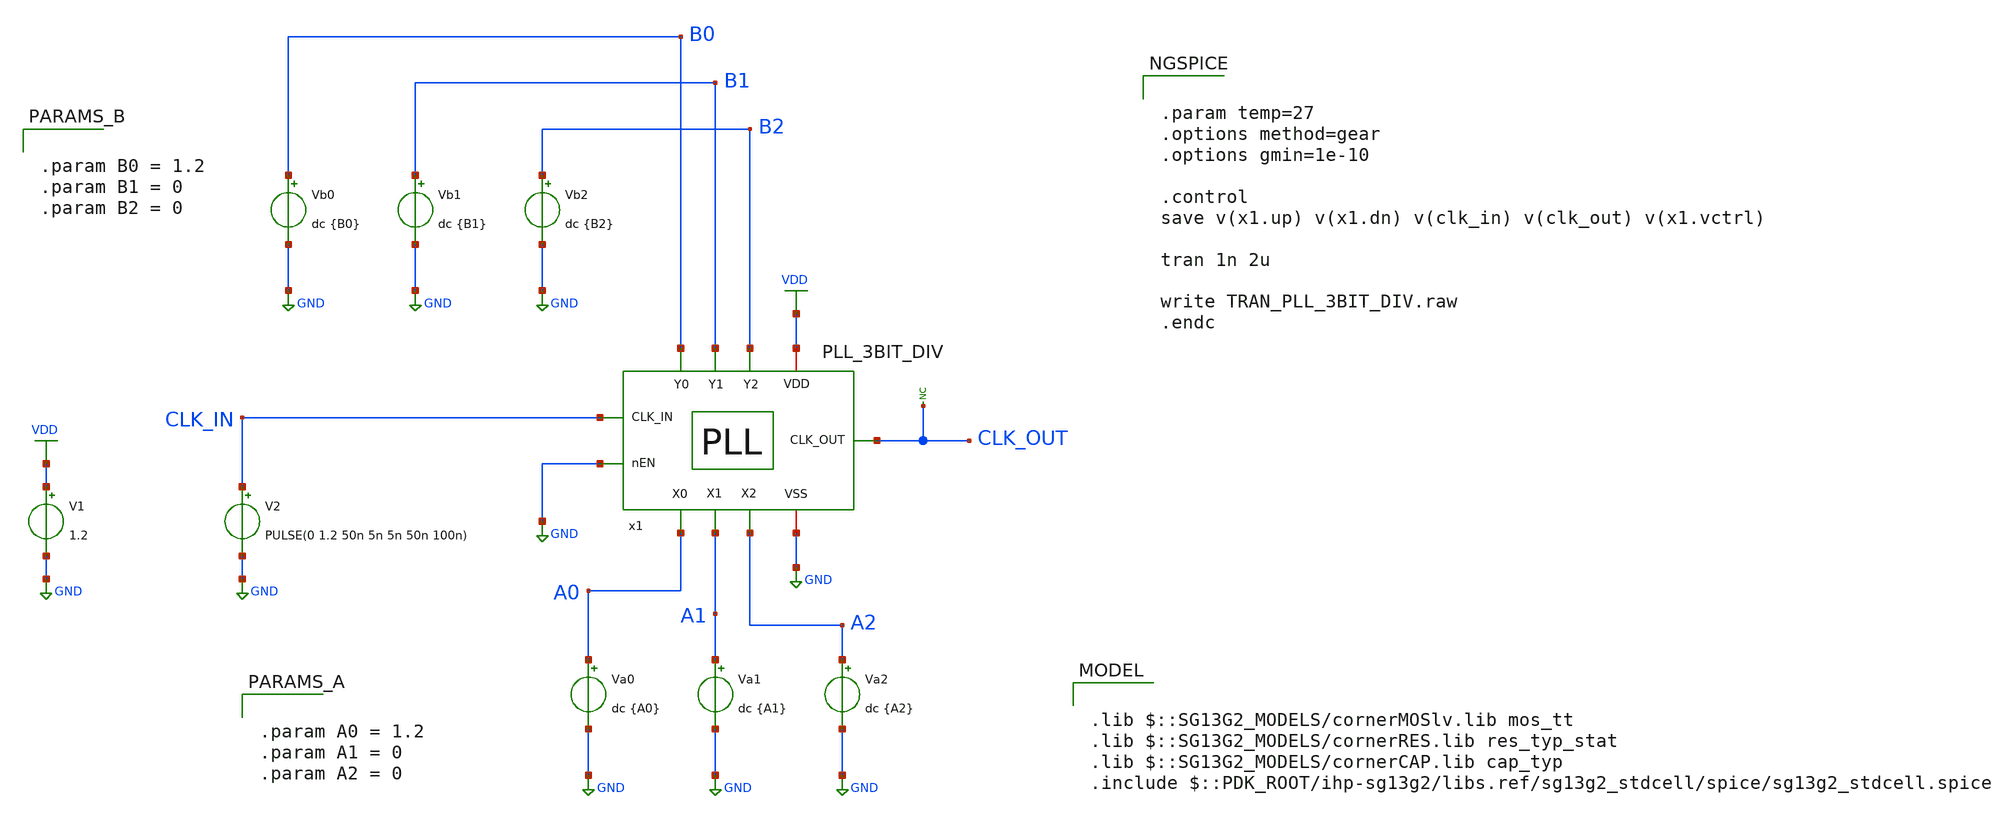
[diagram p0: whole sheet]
** sch_path: 30_MHz_Fractional_N_PLL/design_data/xschem/PLL_3BIT_DIV_TB.sch

.lib $::SG13G2_MODELS/cornerMOSlv.lib mos_tt
.lib $::SG13G2_MODELS/cornerRES.lib res_typ_stat
.lib $::SG13G2_MODELS/cornerCAP.lib cap_typ
.include $::PDK_ROOT/ihp-sg13g2/libs.ref/sg13g2_stdcell/spice/sg13g2_stdcell.spice

**.subckt PLL_3BIT_DIV_TB
V1 VDD GND 1.2
V2 CLK_IN GND PULSE(0 1.2 50n 5n 5n 50n 100n)
Va0 A0 GND dc {A0}
Va1 A1 GND dc {A1}
* noconn CLK_OUT
Va2 A2 GND dc {A2}
Vb0 B0 GND dc {B0}
Vb1 B1 GND dc {B1}
Vb2 B2 GND dc {B2}
x1 CLK_IN CLK_OUT B0 B2 B1 VDD GND GND A1 A2 A0 PLL_3BIT_DIV
**** begin user architecture code


.param temp=27
.options method=gear
.options gmin=1e-10

.control
save v(x1.up) v(x1.dn) v(clk_in) v(clk_out) v(x1.vctrl)

tran 1n 2u

write TRAN_PLL_3BIT_DIV.raw
.endc





.param A0 = 1.2
.param A1 = 0
.param A2 = 0




.param B0 = 1.2
.param B1 = 0
.param B2 = 0




.ic V(VDD) = 1.2
.ic V(x1.up) = 0
.ic V(x1.dn) = 0
.ic V(x1.vctrl) = 0.6


**** end user architecture code
**.ends
.GLOBAL GND
.GLOBAL VDD
.end
